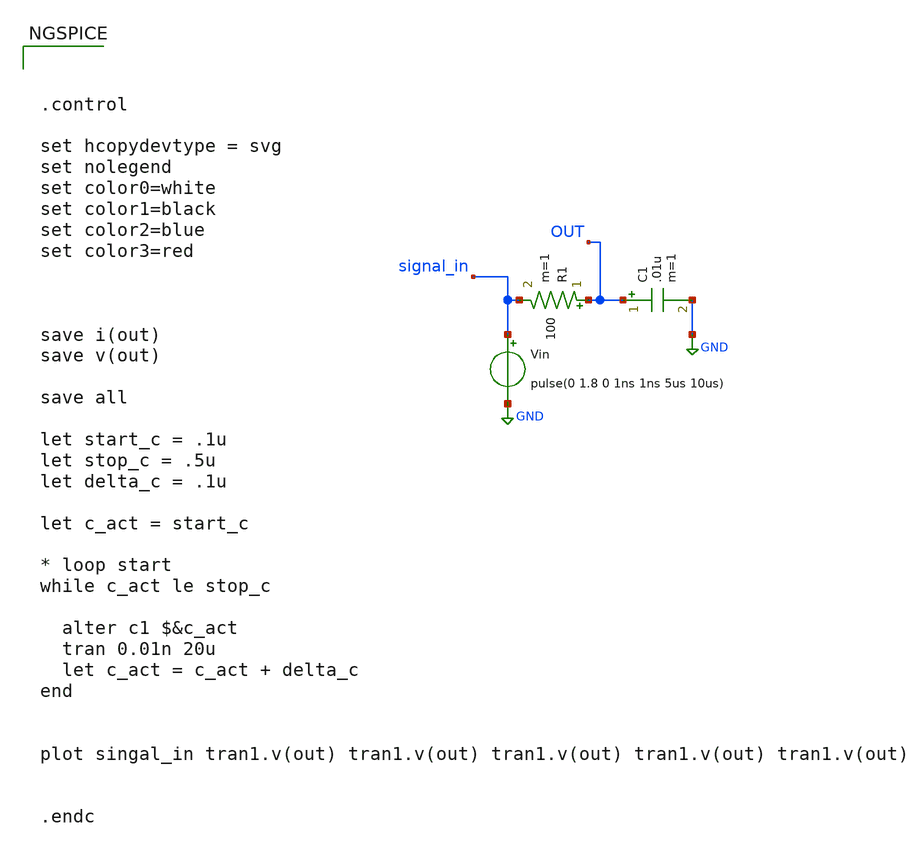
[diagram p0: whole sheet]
** sch_path: sweep_params/untitled.sch
**.subckt untitled
R1 OUT signal_in 100 m=1
C1 OUT GND .01u m=1
Vin signal_in GND pulse(0 1.8 0 1ns 1ns 5us 10us)
**** begin user architecture code

** opencircuitdesign pdks install
.lib $::SKYWATER_MODELS/sky130.lib.spice tt





.control

set hcopydevtype = svg
set nolegend
set color0=white
set color1=black
set color2=blue
set color3=red



save i(out)
save v(out)

save all

let start_c = .1u
let stop_c = .5u
let delta_c = .1u

let c_act = start_c

* loop start
while c_act le stop_c

  alter c1 $&c_act
  tran 0.01n 20u
  let c_act = c_act + delta_c
end


plot singal_in tran1.v(out) tran1.v(out) tran1.v(out) tran1.v(out) tran1.v(out)


.endc



**** end user architecture code
**.ends
.GLOBAL GND
.end
